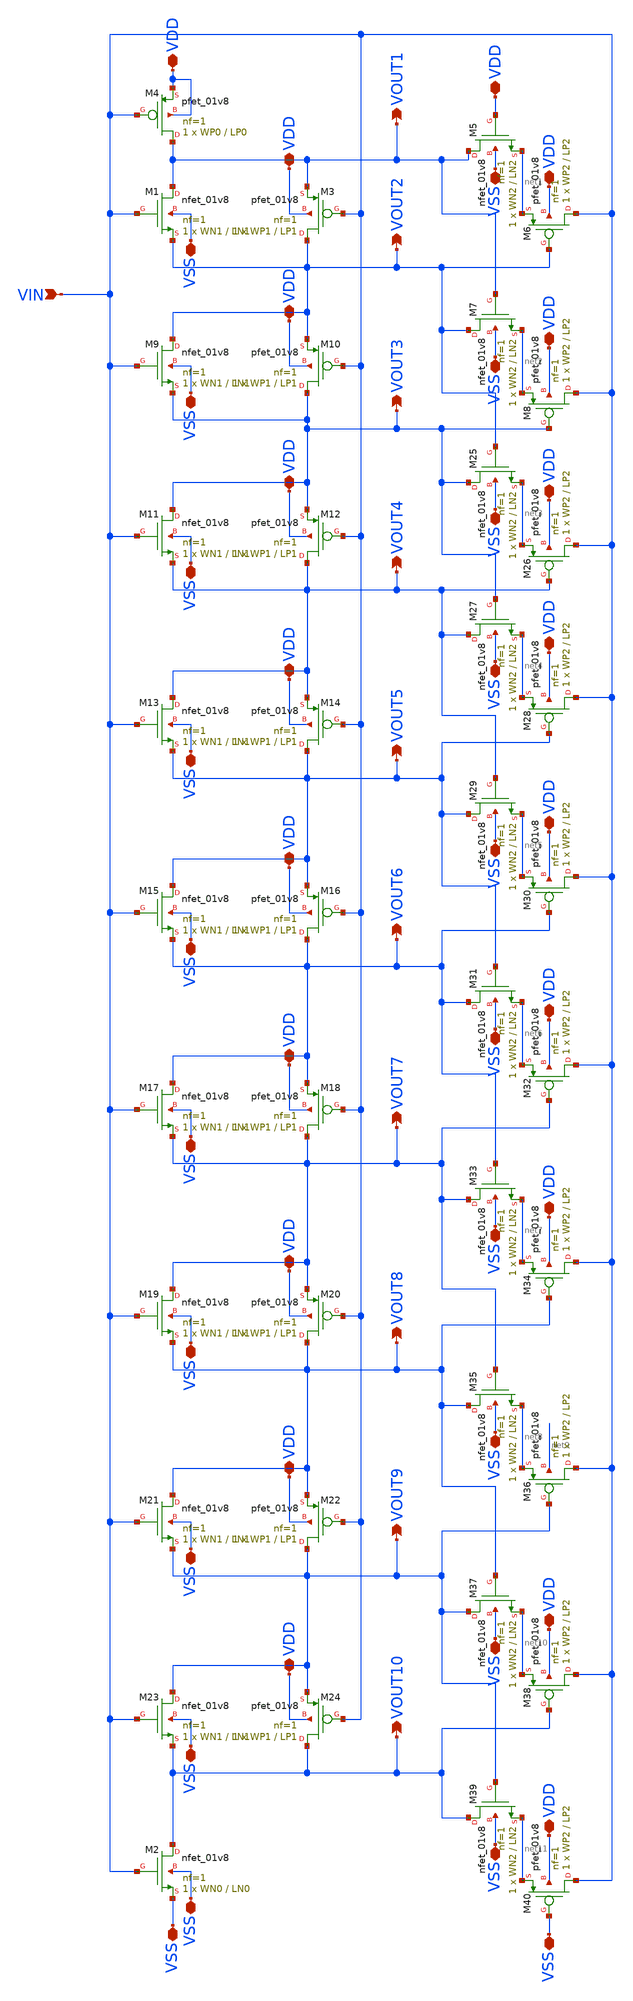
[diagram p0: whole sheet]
** sch_path: LIQAF circuit/10-Stage/MSM-10.sch
**.subckt MSM-10 VIN VDD VDD VDD VDD VDD VDD VDD VDD VDD VDD VDD VDD VDD VDD VDD VDD VDD VDD VDD VDD
*+ VSS VSS VSS VSS VSS VSS VSS VSS VSS VSS VSS VSS VSS VSS VSS VSS VSS VSS VSS VSS VSS VSS VOUT1 VOUT2
*+ VOUT3 VOUT4 VOUT5 VOUT6 VOUT7 VOUT8 VOUT9 VOUT10
*.ipin VIN
*.iopin VDD
*.iopin VDD
*.iopin VDD
*.iopin VDD
*.iopin VDD
*.iopin VDD
*.iopin VDD
*.iopin VDD
*.iopin VDD
*.iopin VDD
*.iopin VDD
*.iopin VDD
*.iopin VDD
*.iopin VDD
*.iopin VDD
*.iopin VDD
*.iopin VDD
*.iopin VDD
*.iopin VDD
*.iopin VDD
*.iopin VSS
*.iopin VSS
*.iopin VSS
*.iopin VSS
*.iopin VSS
*.iopin VSS
*.iopin VSS
*.iopin VSS
*.iopin VSS
*.iopin VSS
*.iopin VSS
*.iopin VSS
*.iopin VSS
*.iopin VSS
*.iopin VSS
*.iopin VSS
*.iopin VSS
*.iopin VSS
*.iopin VSS
*.iopin VSS
*.iopin VSS
*.iopin VSS
*.opin VOUT1
*.opin VOUT2
*.opin VOUT3
*.opin VOUT4
*.opin VOUT5
*.opin VOUT6
*.opin VOUT7
*.opin VOUT8
*.opin VOUT9
*.opin VOUT10
XM1 VOUT1 VIN VOUT2 VSS sky130_fd_pr__nfet_01v8 L=LN1 W=WN1 nf=1 ad='int((nf+1)/2) * W/nf * 0.29' as='int((nf+2)/2) * W/nf * 0.29'
+ pd='2*int((nf+1)/2) * (W/nf + 0.29)' ps='2*int((nf+2)/2) * (W/nf + 0.29)' nrd='0.29 / W' nrs='0.29 / W'
+ sa=0 sb=0 sd=0 mult=1 m=1
XM2 VOUT10 VIN VSS VSS sky130_fd_pr__nfet_01v8 L=LN0 W=WN0 nf=1 ad='int((nf+1)/2) * W/nf * 0.29' as='int((nf+2)/2) * W/nf * 0.29'
+ pd='2*int((nf+1)/2) * (W/nf + 0.29)' ps='2*int((nf+2)/2) * (W/nf + 0.29)' nrd='0.29 / W' nrs='0.29 / W'
+ sa=0 sb=0 sd=0 mult=1 m=1
XM3 VOUT2 VIN VOUT1 VDD sky130_fd_pr__pfet_01v8 L=LP1 W=WP1 nf=1 ad='int((nf+1)/2) * W/nf * 0.29' as='int((nf+2)/2) * W/nf * 0.29'
+ pd='2*int((nf+1)/2) * (W/nf + 0.29)' ps='2*int((nf+2)/2) * (W/nf + 0.29)' nrd='0.29 / W' nrs='0.29 / W'
+ sa=0 sb=0 sd=0 mult=1 m=1
XM4 VOUT1 VIN VDD VDD sky130_fd_pr__pfet_01v8 L=LP0 W=WP0 nf=1 ad='int((nf+1)/2) * W/nf * 0.29' as='int((nf+2)/2) * W/nf * 0.29'
+ pd='2*int((nf+1)/2) * (W/nf + 0.29)' ps='2*int((nf+2)/2) * (W/nf + 0.29)' nrd='0.29 / W' nrs='0.29 / W'
+ sa=0 sb=0 sd=0 mult=1 m=1
XM5 VOUT1 VDD net1 VSS sky130_fd_pr__nfet_01v8 L=LN2 W=WN2 nf=1 ad='int((nf+1)/2) * W/nf * 0.29' as='int((nf+2)/2) * W/nf * 0.29'
+ pd='2*int((nf+1)/2) * (W/nf + 0.29)' ps='2*int((nf+2)/2) * (W/nf + 0.29)' nrd='0.29 / W' nrs='0.29 / W'
+ sa=0 sb=0 sd=0 mult=1 m=1
XM6 VIN VOUT2 net1 VDD sky130_fd_pr__pfet_01v8 L=LP2 W=WP2 nf=1 ad='int((nf+1)/2) * W/nf * 0.29' as='int((nf+2)/2) * W/nf * 0.29'
+ pd='2*int((nf+1)/2) * (W/nf + 0.29)' ps='2*int((nf+2)/2) * (W/nf + 0.29)' nrd='0.29 / W' nrs='0.29 / W'
+ sa=0 sb=0 sd=0 mult=1 m=1
XM7 VOUT2 VOUT1 net2 VSS sky130_fd_pr__nfet_01v8 L=LN2 W=WN2 nf=1 ad='int((nf+1)/2) * W/nf * 0.29' as='int((nf+2)/2) * W/nf * 0.29'
+ pd='2*int((nf+1)/2) * (W/nf + 0.29)' ps='2*int((nf+2)/2) * (W/nf + 0.29)' nrd='0.29 / W' nrs='0.29 / W'
+ sa=0 sb=0 sd=0 mult=1 m=1
XM8 VIN VOUT3 net2 VDD sky130_fd_pr__pfet_01v8 L=LP2 W=WP2 nf=1 ad='int((nf+1)/2) * W/nf * 0.29' as='int((nf+2)/2) * W/nf * 0.29'
+ pd='2*int((nf+1)/2) * (W/nf + 0.29)' ps='2*int((nf+2)/2) * (W/nf + 0.29)' nrd='0.29 / W' nrs='0.29 / W'
+ sa=0 sb=0 sd=0 mult=1 m=1
XM9 VOUT2 VIN VOUT3 VSS sky130_fd_pr__nfet_01v8 L=LN1 W=WN1 nf=1 ad='int((nf+1)/2) * W/nf * 0.29' as='int((nf+2)/2) * W/nf * 0.29'
+ pd='2*int((nf+1)/2) * (W/nf + 0.29)' ps='2*int((nf+2)/2) * (W/nf + 0.29)' nrd='0.29 / W' nrs='0.29 / W'
+ sa=0 sb=0 sd=0 mult=1 m=1
XM10 VOUT3 VIN VOUT2 VDD sky130_fd_pr__pfet_01v8 L=LP1 W=WP1 nf=1 ad='int((nf+1)/2) * W/nf * 0.29' as='int((nf+2)/2) * W/nf * 0.29'
+ pd='2*int((nf+1)/2) * (W/nf + 0.29)' ps='2*int((nf+2)/2) * (W/nf + 0.29)' nrd='0.29 / W' nrs='0.29 / W'
+ sa=0 sb=0 sd=0 mult=1 m=1
XM11 VOUT3 VIN VOUT4 VSS sky130_fd_pr__nfet_01v8 L=LN1 W=WN1 nf=1 ad='int((nf+1)/2) * W/nf * 0.29' as='int((nf+2)/2) * W/nf * 0.29'
+ pd='2*int((nf+1)/2) * (W/nf + 0.29)' ps='2*int((nf+2)/2) * (W/nf + 0.29)' nrd='0.29 / W' nrs='0.29 / W'
+ sa=0 sb=0 sd=0 mult=1 m=1
XM12 VOUT4 VIN VOUT3 VDD sky130_fd_pr__pfet_01v8 L=LP1 W=WP1 nf=1 ad='int((nf+1)/2) * W/nf * 0.29' as='int((nf+2)/2) * W/nf * 0.29'
+ pd='2*int((nf+1)/2) * (W/nf + 0.29)' ps='2*int((nf+2)/2) * (W/nf + 0.29)' nrd='0.29 / W' nrs='0.29 / W'
+ sa=0 sb=0 sd=0 mult=1 m=1
XM13 VOUT4 VIN VOUT5 VSS sky130_fd_pr__nfet_01v8 L=LN1 W=WN1 nf=1 ad='int((nf+1)/2) * W/nf * 0.29' as='int((nf+2)/2) * W/nf * 0.29'
+ pd='2*int((nf+1)/2) * (W/nf + 0.29)' ps='2*int((nf+2)/2) * (W/nf + 0.29)' nrd='0.29 / W' nrs='0.29 / W'
+ sa=0 sb=0 sd=0 mult=1 m=1
XM14 VOUT5 VIN VOUT4 VDD sky130_fd_pr__pfet_01v8 L=LP1 W=WP1 nf=1 ad='int((nf+1)/2) * W/nf * 0.29' as='int((nf+2)/2) * W/nf * 0.29'
+ pd='2*int((nf+1)/2) * (W/nf + 0.29)' ps='2*int((nf+2)/2) * (W/nf + 0.29)' nrd='0.29 / W' nrs='0.29 / W'
+ sa=0 sb=0 sd=0 mult=1 m=1
XM15 VOUT5 VIN VOUT6 VSS sky130_fd_pr__nfet_01v8 L=LN1 W=WN1 nf=1 ad='int((nf+1)/2) * W/nf * 0.29' as='int((nf+2)/2) * W/nf * 0.29'
+ pd='2*int((nf+1)/2) * (W/nf + 0.29)' ps='2*int((nf+2)/2) * (W/nf + 0.29)' nrd='0.29 / W' nrs='0.29 / W'
+ sa=0 sb=0 sd=0 mult=1 m=1
XM16 VOUT6 VIN VOUT5 VDD sky130_fd_pr__pfet_01v8 L=LP1 W=WP1 nf=1 ad='int((nf+1)/2) * W/nf * 0.29' as='int((nf+2)/2) * W/nf * 0.29'
+ pd='2*int((nf+1)/2) * (W/nf + 0.29)' ps='2*int((nf+2)/2) * (W/nf + 0.29)' nrd='0.29 / W' nrs='0.29 / W'
+ sa=0 sb=0 sd=0 mult=1 m=1
XM17 VOUT6 VIN VOUT7 VSS sky130_fd_pr__nfet_01v8 L=LN1 W=WN1 nf=1 ad='int((nf+1)/2) * W/nf * 0.29' as='int((nf+2)/2) * W/nf * 0.29'
+ pd='2*int((nf+1)/2) * (W/nf + 0.29)' ps='2*int((nf+2)/2) * (W/nf + 0.29)' nrd='0.29 / W' nrs='0.29 / W'
+ sa=0 sb=0 sd=0 mult=1 m=1
XM18 VOUT7 VIN VOUT6 VDD sky130_fd_pr__pfet_01v8 L=LP1 W=WP1 nf=1 ad='int((nf+1)/2) * W/nf * 0.29' as='int((nf+2)/2) * W/nf * 0.29'
+ pd='2*int((nf+1)/2) * (W/nf + 0.29)' ps='2*int((nf+2)/2) * (W/nf + 0.29)' nrd='0.29 / W' nrs='0.29 / W'
+ sa=0 sb=0 sd=0 mult=1 m=1
XM19 VOUT7 VIN VOUT8 VSS sky130_fd_pr__nfet_01v8 L=LN1 W=WN1 nf=1 ad='int((nf+1)/2) * W/nf * 0.29' as='int((nf+2)/2) * W/nf * 0.29'
+ pd='2*int((nf+1)/2) * (W/nf + 0.29)' ps='2*int((nf+2)/2) * (W/nf + 0.29)' nrd='0.29 / W' nrs='0.29 / W'
+ sa=0 sb=0 sd=0 mult=1 m=1
XM20 VOUT8 VIN VOUT7 VDD sky130_fd_pr__pfet_01v8 L=LP1 W=WP1 nf=1 ad='int((nf+1)/2) * W/nf * 0.29' as='int((nf+2)/2) * W/nf * 0.29'
+ pd='2*int((nf+1)/2) * (W/nf + 0.29)' ps='2*int((nf+2)/2) * (W/nf + 0.29)' nrd='0.29 / W' nrs='0.29 / W'
+ sa=0 sb=0 sd=0 mult=1 m=1
XM21 VOUT8 VIN VOUT9 VSS sky130_fd_pr__nfet_01v8 L=LN1 W=WN1 nf=1 ad='int((nf+1)/2) * W/nf * 0.29' as='int((nf+2)/2) * W/nf * 0.29'
+ pd='2*int((nf+1)/2) * (W/nf + 0.29)' ps='2*int((nf+2)/2) * (W/nf + 0.29)' nrd='0.29 / W' nrs='0.29 / W'
+ sa=0 sb=0 sd=0 mult=1 m=1
XM22 VOUT9 VIN VOUT8 VDD sky130_fd_pr__pfet_01v8 L=LP1 W=WP1 nf=1 ad='int((nf+1)/2) * W/nf * 0.29' as='int((nf+2)/2) * W/nf * 0.29'
+ pd='2*int((nf+1)/2) * (W/nf + 0.29)' ps='2*int((nf+2)/2) * (W/nf + 0.29)' nrd='0.29 / W' nrs='0.29 / W'
+ sa=0 sb=0 sd=0 mult=1 m=1
XM23 VOUT9 VIN VOUT10 VSS sky130_fd_pr__nfet_01v8 L=LN1 W=WN1 nf=1 ad='int((nf+1)/2) * W/nf * 0.29' as='int((nf+2)/2) * W/nf * 0.29'
+ pd='2*int((nf+1)/2) * (W/nf + 0.29)' ps='2*int((nf+2)/2) * (W/nf + 0.29)' nrd='0.29 / W' nrs='0.29 / W'
+ sa=0 sb=0 sd=0 mult=1 m=1
XM24 VOUT10 VIN VOUT9 VDD sky130_fd_pr__pfet_01v8 L=LP1 W=WP1 nf=1 ad='int((nf+1)/2) * W/nf * 0.29' as='int((nf+2)/2) * W/nf * 0.29'
+ pd='2*int((nf+1)/2) * (W/nf + 0.29)' ps='2*int((nf+2)/2) * (W/nf + 0.29)' nrd='0.29 / W' nrs='0.29 / W'
+ sa=0 sb=0 sd=0 mult=1 m=1
XM25 VOUT3 VOUT2 net3 VSS sky130_fd_pr__nfet_01v8 L=LN2 W=WN2 nf=1 ad='int((nf+1)/2) * W/nf * 0.29' as='int((nf+2)/2) * W/nf * 0.29'
+ pd='2*int((nf+1)/2) * (W/nf + 0.29)' ps='2*int((nf+2)/2) * (W/nf + 0.29)' nrd='0.29 / W' nrs='0.29 / W'
+ sa=0 sb=0 sd=0 mult=1 m=1
XM26 VIN VOUT4 net3 VDD sky130_fd_pr__pfet_01v8 L=LP2 W=WP2 nf=1 ad='int((nf+1)/2) * W/nf * 0.29' as='int((nf+2)/2) * W/nf * 0.29'
+ pd='2*int((nf+1)/2) * (W/nf + 0.29)' ps='2*int((nf+2)/2) * (W/nf + 0.29)' nrd='0.29 / W' nrs='0.29 / W'
+ sa=0 sb=0 sd=0 mult=1 m=1
XM27 VOUT4 VOUT3 net4 VSS sky130_fd_pr__nfet_01v8 L=LN2 W=WN2 nf=1 ad='int((nf+1)/2) * W/nf * 0.29' as='int((nf+2)/2) * W/nf * 0.29'
+ pd='2*int((nf+1)/2) * (W/nf + 0.29)' ps='2*int((nf+2)/2) * (W/nf + 0.29)' nrd='0.29 / W' nrs='0.29 / W'
+ sa=0 sb=0 sd=0 mult=1 m=1
XM28 VIN VOUT5 net4 VDD sky130_fd_pr__pfet_01v8 L=LP2 W=WP2 nf=1 ad='int((nf+1)/2) * W/nf * 0.29' as='int((nf+2)/2) * W/nf * 0.29'
+ pd='2*int((nf+1)/2) * (W/nf + 0.29)' ps='2*int((nf+2)/2) * (W/nf + 0.29)' nrd='0.29 / W' nrs='0.29 / W'
+ sa=0 sb=0 sd=0 mult=1 m=1
XM29 VOUT5 VOUT4 net5 VSS sky130_fd_pr__nfet_01v8 L=LN2 W=WN2 nf=1 ad='int((nf+1)/2) * W/nf * 0.29' as='int((nf+2)/2) * W/nf * 0.29'
+ pd='2*int((nf+1)/2) * (W/nf + 0.29)' ps='2*int((nf+2)/2) * (W/nf + 0.29)' nrd='0.29 / W' nrs='0.29 / W'
+ sa=0 sb=0 sd=0 mult=1 m=1
XM30 VIN VOUT6 net5 VDD sky130_fd_pr__pfet_01v8 L=LP2 W=WP2 nf=1 ad='int((nf+1)/2) * W/nf * 0.29' as='int((nf+2)/2) * W/nf * 0.29'
+ pd='2*int((nf+1)/2) * (W/nf + 0.29)' ps='2*int((nf+2)/2) * (W/nf + 0.29)' nrd='0.29 / W' nrs='0.29 / W'
+ sa=0 sb=0 sd=0 mult=1 m=1
XM31 VOUT6 VOUT5 net6 VSS sky130_fd_pr__nfet_01v8 L=LN2 W=WN2 nf=1 ad='int((nf+1)/2) * W/nf * 0.29' as='int((nf+2)/2) * W/nf * 0.29'
+ pd='2*int((nf+1)/2) * (W/nf + 0.29)' ps='2*int((nf+2)/2) * (W/nf + 0.29)' nrd='0.29 / W' nrs='0.29 / W'
+ sa=0 sb=0 sd=0 mult=1 m=1
XM32 VIN VOUT7 net6 VDD sky130_fd_pr__pfet_01v8 L=LP2 W=WP2 nf=1 ad='int((nf+1)/2) * W/nf * 0.29' as='int((nf+2)/2) * W/nf * 0.29'
+ pd='2*int((nf+1)/2) * (W/nf + 0.29)' ps='2*int((nf+2)/2) * (W/nf + 0.29)' nrd='0.29 / W' nrs='0.29 / W'
+ sa=0 sb=0 sd=0 mult=1 m=1
XM33 VOUT7 VOUT6 net7 VSS sky130_fd_pr__nfet_01v8 L=LN2 W=WN2 nf=1 ad='int((nf+1)/2) * W/nf * 0.29' as='int((nf+2)/2) * W/nf * 0.29'
+ pd='2*int((nf+1)/2) * (W/nf + 0.29)' ps='2*int((nf+2)/2) * (W/nf + 0.29)' nrd='0.29 / W' nrs='0.29 / W'
+ sa=0 sb=0 sd=0 mult=1 m=1
XM34 VIN VOUT8 net7 VDD sky130_fd_pr__pfet_01v8 L=LP2 W=WP2 nf=1 ad='int((nf+1)/2) * W/nf * 0.29' as='int((nf+2)/2) * W/nf * 0.29'
+ pd='2*int((nf+1)/2) * (W/nf + 0.29)' ps='2*int((nf+2)/2) * (W/nf + 0.29)' nrd='0.29 / W' nrs='0.29 / W'
+ sa=0 sb=0 sd=0 mult=1 m=1
XM35 VOUT8 VOUT7 net8 VSS sky130_fd_pr__nfet_01v8 L=LN2 W=WN2 nf=1 ad='int((nf+1)/2) * W/nf * 0.29' as='int((nf+2)/2) * W/nf * 0.29'
+ pd='2*int((nf+1)/2) * (W/nf + 0.29)' ps='2*int((nf+2)/2) * (W/nf + 0.29)' nrd='0.29 / W' nrs='0.29 / W'
+ sa=0 sb=0 sd=0 mult=1 m=1
XM36 VIN VOUT9 net8 net9 sky130_fd_pr__pfet_01v8 L=LP2 W=WP2 nf=1 ad='int((nf+1)/2) * W/nf * 0.29' as='int((nf+2)/2) * W/nf * 0.29'
+ pd='2*int((nf+1)/2) * (W/nf + 0.29)' ps='2*int((nf+2)/2) * (W/nf + 0.29)' nrd='0.29 / W' nrs='0.29 / W'
+ sa=0 sb=0 sd=0 mult=1 m=1
XM37 VOUT9 VOUT8 net10 VSS sky130_fd_pr__nfet_01v8 L=LN2 W=WN2 nf=1 ad='int((nf+1)/2) * W/nf * 0.29'
+ as='int((nf+2)/2) * W/nf * 0.29' pd='2*int((nf+1)/2) * (W/nf + 0.29)' ps='2*int((nf+2)/2) * (W/nf + 0.29)'
+ nrd='0.29 / W' nrs='0.29 / W' sa=0 sb=0 sd=0 mult=1 m=1
XM38 VIN VOUT10 net10 VDD sky130_fd_pr__pfet_01v8 L=LP2 W=WP2 nf=1 ad='int((nf+1)/2) * W/nf * 0.29' as='int((nf+2)/2) * W/nf * 0.29'
+ pd='2*int((nf+1)/2) * (W/nf + 0.29)' ps='2*int((nf+2)/2) * (W/nf + 0.29)' nrd='0.29 / W' nrs='0.29 / W'
+ sa=0 sb=0 sd=0 mult=1 m=1
XM39 VOUT10 VOUT9 net11 VSS sky130_fd_pr__nfet_01v8 L=LN2 W=WN2 nf=1 ad='int((nf+1)/2) * W/nf * 0.29'
+ as='int((nf+2)/2) * W/nf * 0.29' pd='2*int((nf+1)/2) * (W/nf + 0.29)' ps='2*int((nf+2)/2) * (W/nf + 0.29)'
+ nrd='0.29 / W' nrs='0.29 / W' sa=0 sb=0 sd=0 mult=1 m=1
XM40 VIN VSS net11 VDD sky130_fd_pr__pfet_01v8 L=LP2 W=WP2 nf=1 ad='int((nf+1)/2) * W/nf * 0.29' as='int((nf+2)/2) * W/nf * 0.29'
+ pd='2*int((nf+1)/2) * (W/nf + 0.29)' ps='2*int((nf+2)/2) * (W/nf + 0.29)' nrd='0.29 / W' nrs='0.29 / W'
+ sa=0 sb=0 sd=0 mult=1 m=1
**.ends
.end
